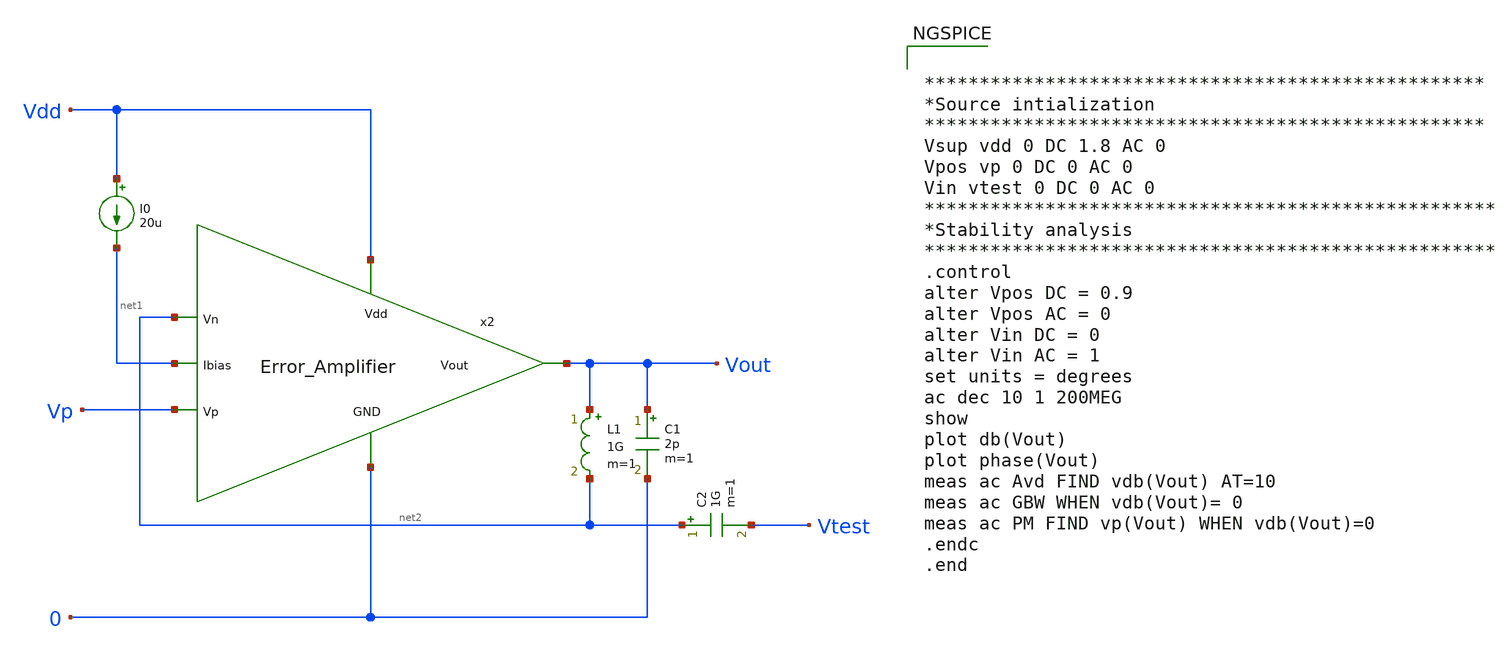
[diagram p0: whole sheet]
** sch_path: Analog_Blocks/LDO/Testbench/LDO_Miller_1.8v_ErAmp_STB.sch
**.subckt LDO_Miller_1.8v_ErAmp_STB
I0 Vdd net1 20u
L1 Vout net2 1G m=1
C2 net2 Vtest 1G m=1
C1 Vout 0 2p m=1
x2 Vdd net2 Vp Vout net1 0 Error_Amplifier
**** begin user architecture code

.include ~/Analog_blocks/models/skywater-pdk/libraries/sky130_fd_pr/latest/cells/nfet_01v8/sky130_fd_pr__nfet_01v8__tt.corner.spice
.include ~/Analog_blocks/models/skywater-pdk/libraries/sky130_fd_pr/latest/cells/nfet_01v8_lvt/sky130_fd_pr__nfet_01v8_lvt__tt.corner.spice
.include ~/Analog_blocks/models/skywater-pdk/libraries/sky130_fd_pr/latest/cells/pfet_01v8/sky130_fd_pr__pfet_01v8__tt.corner.spice
.include ~/Analog_blocks/models/skywater-pdk/libraries/sky130_fd_pr/latest/cells/nfet_03v3_nvt/sky130_fd_pr__nfet_03v3_nvt__tt.corner.spice
.include ~/Analog_blocks/models/skywater-pdk/libraries/sky130_fd_pr/latest/cells/nfet_05v0_nvt/sky130_fd_pr__nfet_05v0_nvt__tt.corner.spice
.include ~/Analog_blocks/models/skywater-pdk/libraries/sky130_fd_pr/latest/cells/esd_nfet_01v8/sky130_fd_pr__esd_nfet_01v8__tt.corner.spice
.include ~/Analog_blocks/models/skywater-pdk/libraries/sky130_fd_pr/latest/cells/pfet_01v8_lvt/sky130_fd_pr__pfet_01v8_lvt__tt.corner.spice
.include ~/Analog_blocks/models/skywater-pdk/libraries/sky130_fd_pr/latest/cells/pfet_01v8_hvt/sky130_fd_pr__pfet_01v8_hvt__tt.corner.spice
.include ~/Analog_blocks/models/skywater-pdk/libraries/sky130_fd_pr/latest/cells/esd_pfet_g5v0d10v5/sky130_fd_pr__esd_pfet_g5v0d10v5__tt.corner.spice
.include ~/Analog_blocks/models/skywater-pdk/libraries/sky130_fd_pr/latest/cells/pfet_g5v0d10v5/sky130_fd_pr__pfet_g5v0d10v5__tt.corner.spice
.include ~/Analog_blocks/models/skywater-pdk/libraries/sky130_fd_pr/latest/cells/pfet_g5v0d16v0/sky130_fd_pr__pfet_g5v0d16v0__tt.corner.spice
.include ~/Analog_blocks/models/skywater-pdk/libraries/sky130_fd_pr/latest/cells/nfet_g5v0d10v5/sky130_fd_pr__nfet_g5v0d10v5__tt.corner.spice
.include ~/Analog_blocks/models/skywater-pdk/libraries/sky130_fd_pr/latest/cells/nfet_g5v0d16v0/sky130_fd_pr__nfet_g5v0d16v0__tt_discrete.corner.spice
.include ~/Analog_blocks/models/skywater-pdk/libraries/sky130_fd_pr/latest/cells/esd_nfet_g5v0d10v5/sky130_fd_pr__esd_nfet_g5v0d10v5__tt.corner.spice
.include ~/Analog_blocks/models/skywater-pdk/libraries/sky130_fd_pr/latest/models/corners/tt/nonfet.spice
* Mismatch parameters
.include ~/Analog_blocks/models/skywater-pdk/libraries/sky130_fd_pr/latest/cells/nfet_01v8/sky130_fd_pr__nfet_01v8__mismatch.corner.spice
.include ~/Analog_blocks/models/skywater-pdk/libraries/sky130_fd_pr/latest/cells/pfet_01v8/sky130_fd_pr__pfet_01v8__mismatch.corner.spice
.include ~/Analog_blocks/models/skywater-pdk/libraries/sky130_fd_pr/latest/cells/nfet_01v8_lvt/sky130_fd_pr__nfet_01v8_lvt__mismatch.corner.spice
.include ~/Analog_blocks/models/skywater-pdk/libraries/sky130_fd_pr/latest/cells/pfet_01v8_lvt/sky130_fd_pr__pfet_01v8_lvt__mismatch.corner.spice
.include ~/Analog_blocks/models/skywater-pdk/libraries/sky130_fd_pr/latest/cells/pfet_01v8_hvt/sky130_fd_pr__pfet_01v8_hvt__mismatch.corner.spice
.include ~/Analog_blocks/models/skywater-pdk/libraries/sky130_fd_pr/latest/cells/nfet_g5v0d10v5/sky130_fd_pr__nfet_g5v0d10v5__mismatch.corner.spice
.include ~/Analog_blocks/models/skywater-pdk/libraries/sky130_fd_pr/latest/cells/pfet_g5v0d10v5/sky130_fd_pr__pfet_g5v0d10v5__mismatch.corner.spice
.include ~/Analog_blocks/models/skywater-pdk/libraries/sky130_fd_pr/latest/cells/nfet_05v0_nvt/sky130_fd_pr__nfet_05v0_nvt__mismatch.corner.spice
.include ~/Analog_blocks/models/skywater-pdk/libraries/sky130_fd_pr/latest/cells/nfet_03v3_nvt/sky130_fd_pr__nfet_03v3_nvt__mismatch.corner.spice
* Resistor
.include ~/Analog_blocks/models/skywater-pdk/libraries/sky130_fd_pr/latest/models/r+c/res_typical__cap_typical.spice
.include ~/Analog_blocks/models/skywater-pdk/libraries/sky130_fd_pr/latest/models/r+c/res_typical__cap_typical__lin.spice
* Special cells
.include ~/Analog_blocks/models/skywater-pdk/libraries/sky130_fd_pr/latest/models/corners/tt/specialized_cells.spice
* All models
.include ~/Analog_blocks/models/skywater-pdk/libraries/sky130_fd_pr/latest/models/all.spice
* Corner
.include ~/Analog_blocks/models/skywater-pdk/libraries/sky130_fd_pr/latest/models/corners/tt/rf.spice



***************************************************
*Source intialization
***************************************************
Vsup vdd 0 DC 1.8 AC 0
Vpos vp 0 DC 0 AC 0
Vin vtest 0 DC 0 AC 0
****************************************************
*Stability analysis
****************************************************
.control
alter Vpos DC = 0.9
alter Vpos AC = 0
alter Vin DC = 0
alter Vin AC = 1
set units = degrees
ac dec 10 1 200MEG
show
plot db(Vout)
plot phase(Vout)
meas ac Avd FIND vdb(Vout) AT=10
meas ac GBW WHEN vdb(Vout)= 0
meas ac PM FIND vp(Vout) WHEN vdb(Vout)=0
.endc
.end


**** end user architecture code
**.ends
.end
